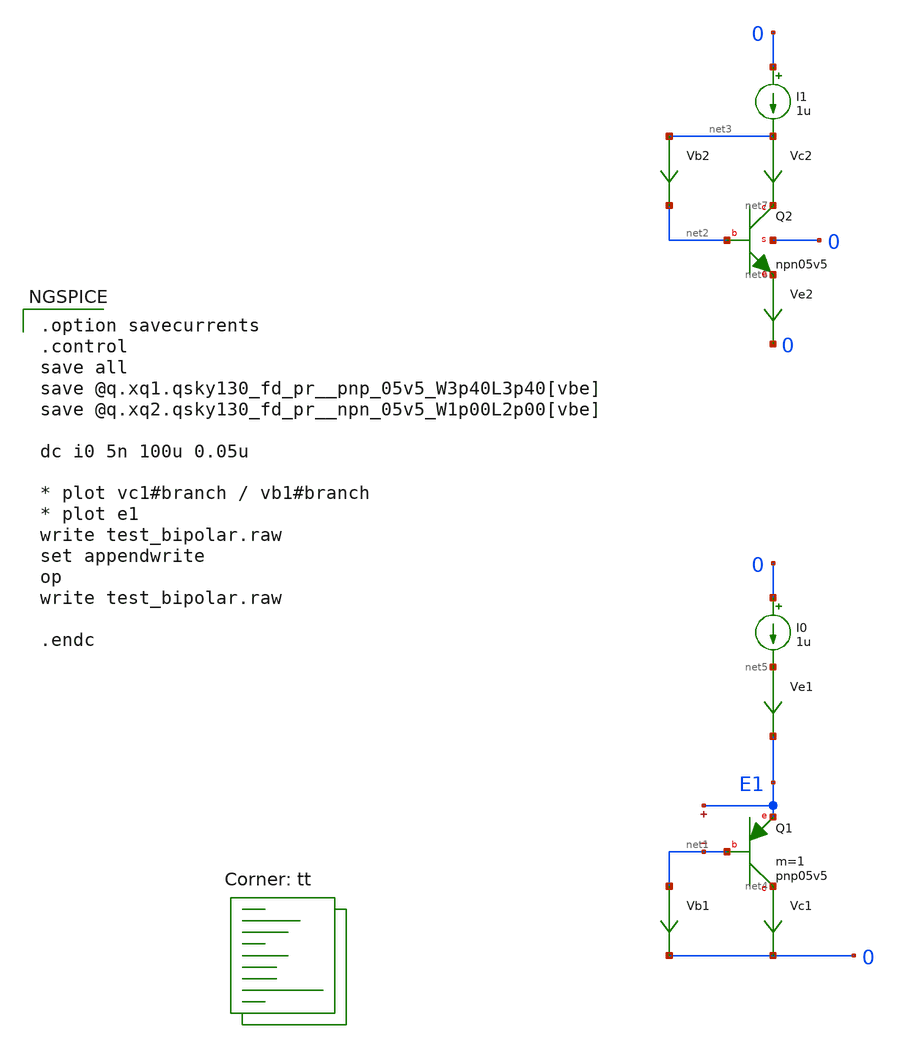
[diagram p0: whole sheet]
** sch_path: sky130_tests/test_bipolar.sch
* Copyright 2021 Stefan Frederik Schippers
* Licensed under the Apache License, Version 2.0 (the "License");
* you may not use this file except in compliance with the License.
* You may obtain a copy of the License at
* https://www.apache.org/licenses/LICENSE-2.0
* Unless required by applicable law or agreed to in writing, software
* distributed under the License is distributed on an "AS IS" BASIS,
* WITHOUT WARRANTIES OR CONDITIONS OF ANY KIND, either express or implied.
* See the License for the specific language governing permissions and
* limitations under the License.
**.subckt test_bipolar
XQ1 net4 net1 E1 sky130_fd_pr__pnp_05v5_W3p40L3p40 m=1
Vc1 net4 0 0
.save i(vc1)
Vb1 net1 0 0
.save i(vb1)
I0 0 net5 1u
Ve1 net5 E1 0
.save i(ve1)
.save v(e1)
.save v(net1)
Ve2 net6 0 0
.save i(ve2)
Vc2 net3 net7 0
.save i(vc2)
Vb2 net3 net2 0
.save i(vb2)
I1 0 net3 1u
XQ2 net7 net2 net6 0 sky130_fd_pr__npn_05v5_w1p00l2p00
**** begin user architecture code

.option savecurrents
.control
save all
save @q.xq1.qsky130_fd_pr__pnp_05v5_W3p40L3p40[vbe]
save @q.xq2.qsky130_fd_pr__npn_05v5_W1p00L2p00[vbe]

dc i0 5n 100u 0.05u

* plot vc1#branch / vb1#branch
* plot e1
write test_bipolar.raw
set appendwrite
op
write test_bipolar.raw

.endc


.lib $::SKYWATER_MODELS/sky130.lib.spice tt
**** end user architecture code
**.ends
.end
